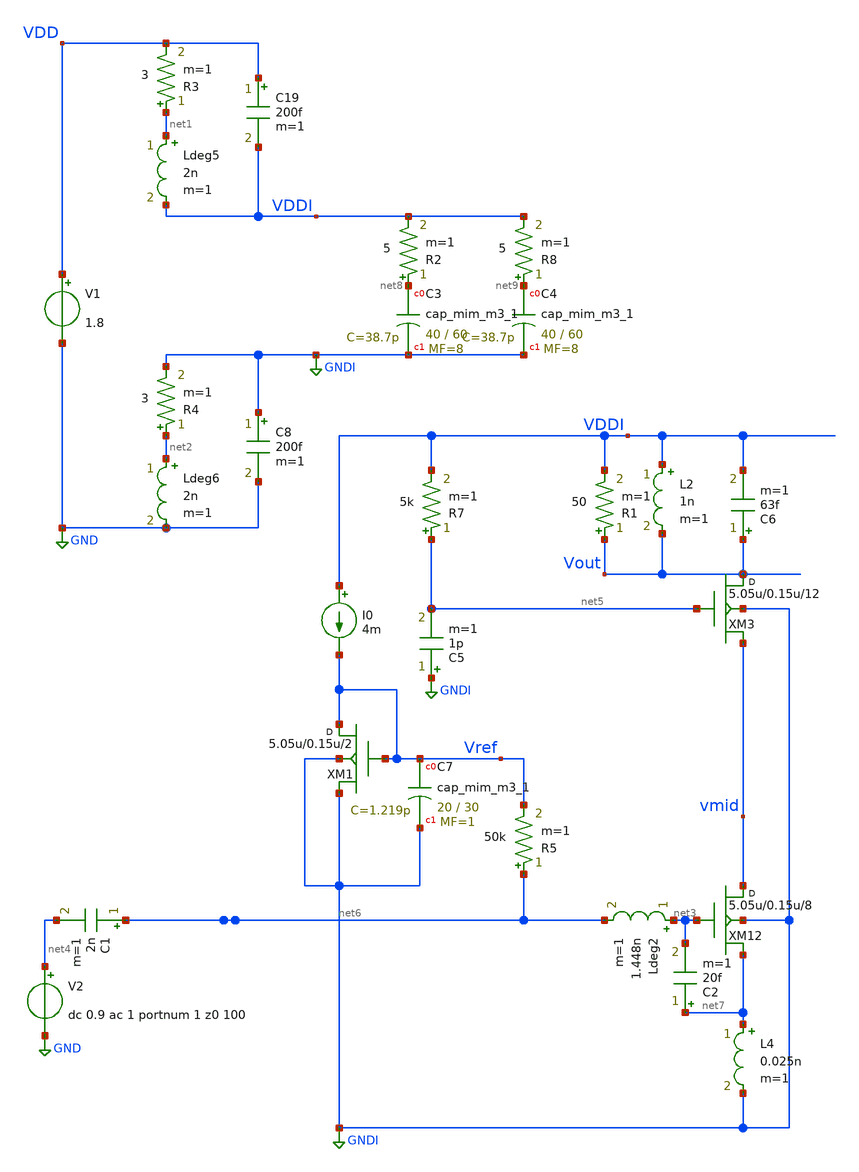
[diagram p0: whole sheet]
** sch_path: xschem/lna/15G_LNA_ac.sch
**.subckt 15G_LNA_ac
V1 VDD GND 1.8
V2 net4 GND dc 0.9 ac 1 portnum 1 z0 100
I0 VDDI Vref 4m
XM1 Vref Vref GNDI GNDI sky130_fd_pr__rf_nfet_01v8_bM04W5p00L0p15_ext w=5.05u l=0.15u m=2
XC7 Vref GNDI sky130_fd_pr__cap_mim_m3_1 W=20 L=30 MF=1 m=1
Ldeg5 net1 VDDI 2n m=1
R3 net1 VDD 3 m=1
Ldeg6 net2 GND 2n m=1
R4 net2 GNDI 3 m=1
XM12 vmid net3 net7 GNDI sky130_fd_pr__rf_nfet_01v8_bM04W5p00L0p15_ext w=5.05u l=0.15u m=8
L2 VDDI Vout 1n m=1
XC3 net8 GNDI sky130_fd_pr__cap_mim_m3_1 W=40 L=60 MF=8 m=8
C8 GNDI GND 200f m=1
C19 VDD VDDI 200f m=1
R2 net8 VDDI 5 m=1
R5 net6 Vref 50k m=1
C1 net6 net4 2n m=1
C6 Vout VDDI 63f m=1
XM3 Vout net5 vmid GNDI sky130_fd_pr__rf_nfet_01v8_bM04W5p00L0p15_ext w=5.05u l=0.15u m=12
Ldeg2 net3 net6 1.448n m=1
XC4 net9 GNDI sky130_fd_pr__cap_mim_m3_1 W=40 L=60 MF=8 m=8
R8 net9 VDDI 5 m=1
L4 net7 GNDI 0.025n m=1
R7 net5 VDDI 5k m=1
C5 GNDI net5 1p m=1
C2 net7 net3 20f m=1
R1 Vout VDDI 50 m=1
**** begin user architecture code


.subckt sky130_fd_pr__rf_nfet_01v8_bM04W5p00L0p15_ext DRAIN GATE SOURCE SUBSTRATE
X0 DRAIN GATE SOURCE SUBSTRATE sky130_fd_pr__nfet_01v8 ad=2.828e+12p pd=2.132e+07u as=4.242e+12p
+ ps=3.198e+07u w=5.05e+06u l=150000u
X1 SOURCE SUBSTRATE SUBSTRATE SUBSTRATE sky130_fd_pr__nfet_01v8 ad=0p pd=0u as=3.03e+12p
+ ps=2.14e+07u w=5.05e+06u l=150000u
X2 SOURCE GATE DRAIN SUBSTRATE sky130_fd_pr__nfet_01v8 ad=0p pd=0u as=0p ps=0u w=5.05e+06u l=150000u
X3 DRAIN GATE SOURCE SUBSTRATE sky130_fd_pr__nfet_01v8 ad=0p pd=0u as=0p ps=0u w=5.05e+06u l=150000u
X4 SUBSTRATE SUBSTRATE SOURCE SUBSTRATE sky130_fd_pr__nfet_01v8 ad=0p pd=0u as=0p ps=0u w=5.05e+06u
+ l=150000u
X5 SOURCE GATE DRAIN SUBSTRATE sky130_fd_pr__nfet_01v8 ad=0p pd=0u as=0p ps=0u w=5.05e+06u l=150000u
.ends
*.sp dec 1000 0.1e9 100e9 1
*.ac dec 1000 0.01e9 100e9
.control
save all
run
display

ac dec 10 10G 100G
let phase = 180/PI*vp(Vout)

plot vdb(Vout) phase
plot phase

.endc



** opencircuitdesign pdks install
.lib $::SKYWATER_MODELS/sky130.lib.spice tt




.param temp=27

.op
.ac dec 10 1 1G
*.tran 0.001 50n 20n

.control
ac dec 10 1 1G
let phase = 180/PI*vp(Vout)

plot vdb(Vout) phase
plot phase

.endc

.save all



**** end user architecture code
**.ends
.GLOBAL GND
.GLOBAL GNDI
.end
